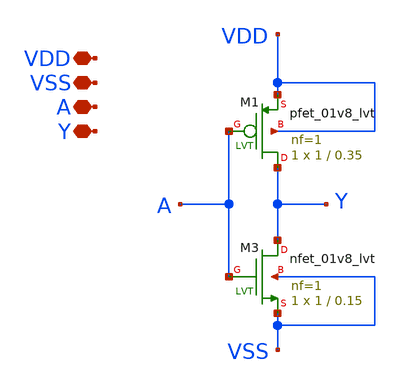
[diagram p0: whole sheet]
** sch_path: inverter/inverter.sch
**.subckt inverter VDD VSS A Y
*.iopin VDD
*.iopin VSS
*.iopin A
*.iopin Y
XM3 Y A VSS VSS sky130_fd_pr__nfet_01v8_lvt L=0.15 W=1 nf=1 ad='int((nf+1)/2) * W/nf * 0.29' as='int((nf+2)/2) * W/nf * 0.29'
+ pd='2*int((nf+1)/2) * (W/nf + 0.29)' ps='2*int((nf+2)/2) * (W/nf + 0.29)' nrd='0.29 / W' nrs='0.29 / W'
+ sa=0 sb=0 sd=0 mult=1 m=1
XM1 Y A VDD VDD sky130_fd_pr__pfet_01v8_lvt L=0.35 W=1 nf=1 ad='int((nf+1)/2) * W/nf * 0.29' as='int((nf+2)/2) * W/nf * 0.29'
+ pd='2*int((nf+1)/2) * (W/nf + 0.29)' ps='2*int((nf+2)/2) * (W/nf + 0.29)' nrd='0.29 / W' nrs='0.29 / W'
+ sa=0 sb=0 sd=0 mult=1 m=1
**** begin user architecture code

** opencircuitdesign pdks install
.lib $::SKYWATER_MODELS/sky130.lib.spice tt


**** end user architecture code
**.ends
.end
